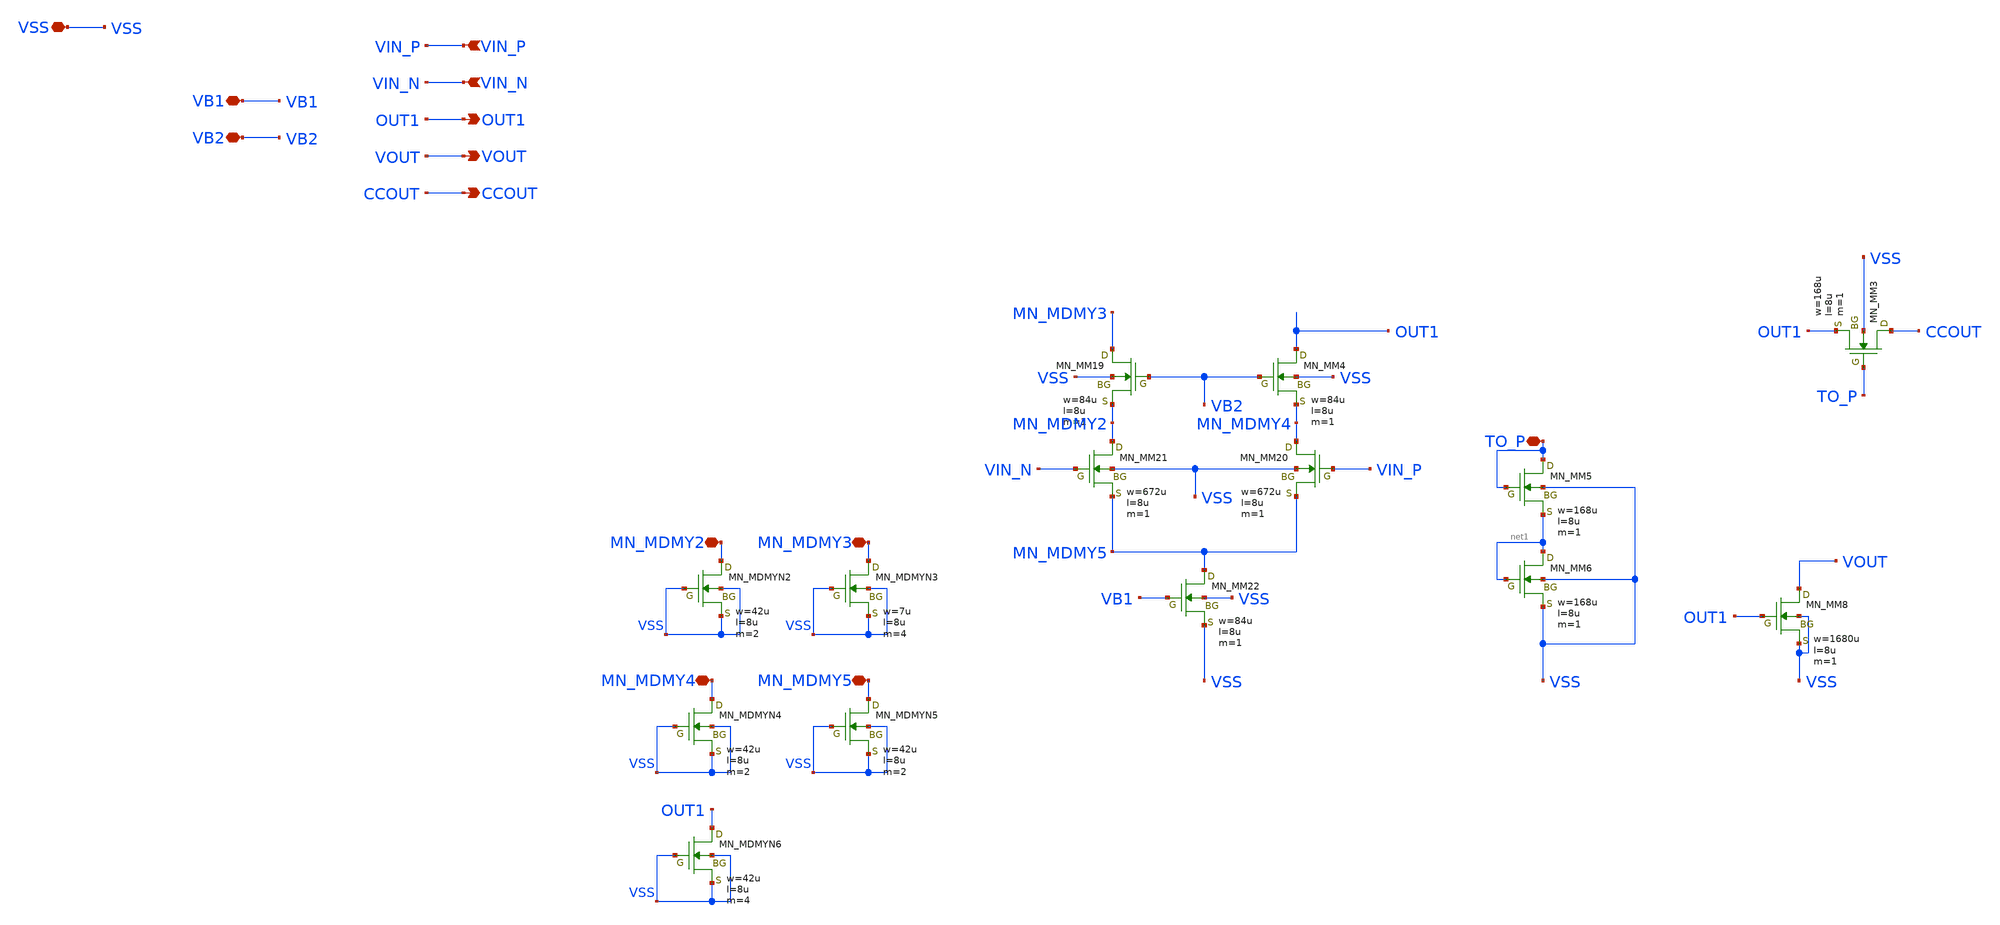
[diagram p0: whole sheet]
** sch_path: member_project/AM_Radio/noritsuna/xschem/DIFF_NMOS.sch
**.subckt DIFF_NMOS VSS VB1 VB2 OUT1 VIN_N VIN_P MN_MDMY2 MN_MDMY3 MN_MDMY4 TO_P MN_MDMY5 VOUT CCOUT
*.iopin VSS
*.iopin VB1
*.iopin VB2
*.opin OUT1
*.ipin VIN_N
*.ipin VIN_P
*.iopin MN_MDMY2
*.iopin MN_MDMY3
*.iopin MN_MDMY4
*.iopin TO_P
*.iopin MN_MDMY5
*.opin VOUT
*.opin CCOUT
MM4 OUT1 VB2 MN_MDMY4 VSS NMOS w=84u l=8u as=0 ad=0 ps=0 pd=0 nrd=0 nrs=0 m=1
MM19 MN_MDMY3 VB2 MN_MDMY2 VSS NMOS w=84u l=8u as=0 ad=0 ps=0 pd=0 nrd=0 nrs=0 m=1
MM20 MN_MDMY4 VIN_P MN_MDMY5 VSS NMOS w=672u l=8u as=0 ad=0 ps=0 pd=0 nrd=0 nrs=0 m=1
MM21 MN_MDMY2 VIN_N MN_MDMY5 VSS NMOS w=672u l=8u as=0 ad=0 ps=0 pd=0 nrd=0 nrs=0 m=1
MM22 MN_MDMY5 VB1 VSS VSS NMOS w=84u l=8u as=0 ad=0 ps=0 pd=0 nrd=0 nrs=0 m=1
XMDMYN2 MN_MDMY2 VSS VSS VSS NMOS w=42u l=8u as=0 ad=0 ps=0 pd=0 nrd=0 nrs=0 m=2
XMDMYN3 MN_MDMY3 VSS VSS VSS NMOS w=7u l=8u as=0 ad=0 ps=0 pd=0 nrd=0 nrs=0 m=4
MM6 net1 net1 VSS VSS NMOS w=168u l=8u as=0 ad=0 ps=0 pd=0 nrd=0 nrs=0 m=1
MM5 TO_P TO_P net1 VSS NMOS w=168u l=8u as=0 ad=0 ps=0 pd=0 nrd=0 nrs=0 m=1
XMDMYN4 MN_MDMY4 VSS VSS VSS NMOS w=42u l=8u as=0 ad=0 ps=0 pd=0 nrd=0 nrs=0 m=2
XMDMYN5 MN_MDMY5 VSS VSS VSS NMOS w=42u l=8u as=0 ad=0 ps=0 pd=0 nrd=0 nrs=0 m=2
MM8 VOUT OUT1 VSS VSS NMOS w=1680u l=8u as=0 ad=0 ps=0 pd=0 nrd=0 nrs=0 m=1
MM3 CCOUT TO_P OUT1 VSS NMOS w=168u l=8u as=0 ad=0 ps=0 pd=0 nrd=0 nrs=0 m=1
XMDMYN6 OUT1 VSS VSS VSS NMOS w=42u l=8u as=0 ad=0 ps=0 pd=0 nrd=0 nrs=0 m=4
**.ends
.end
